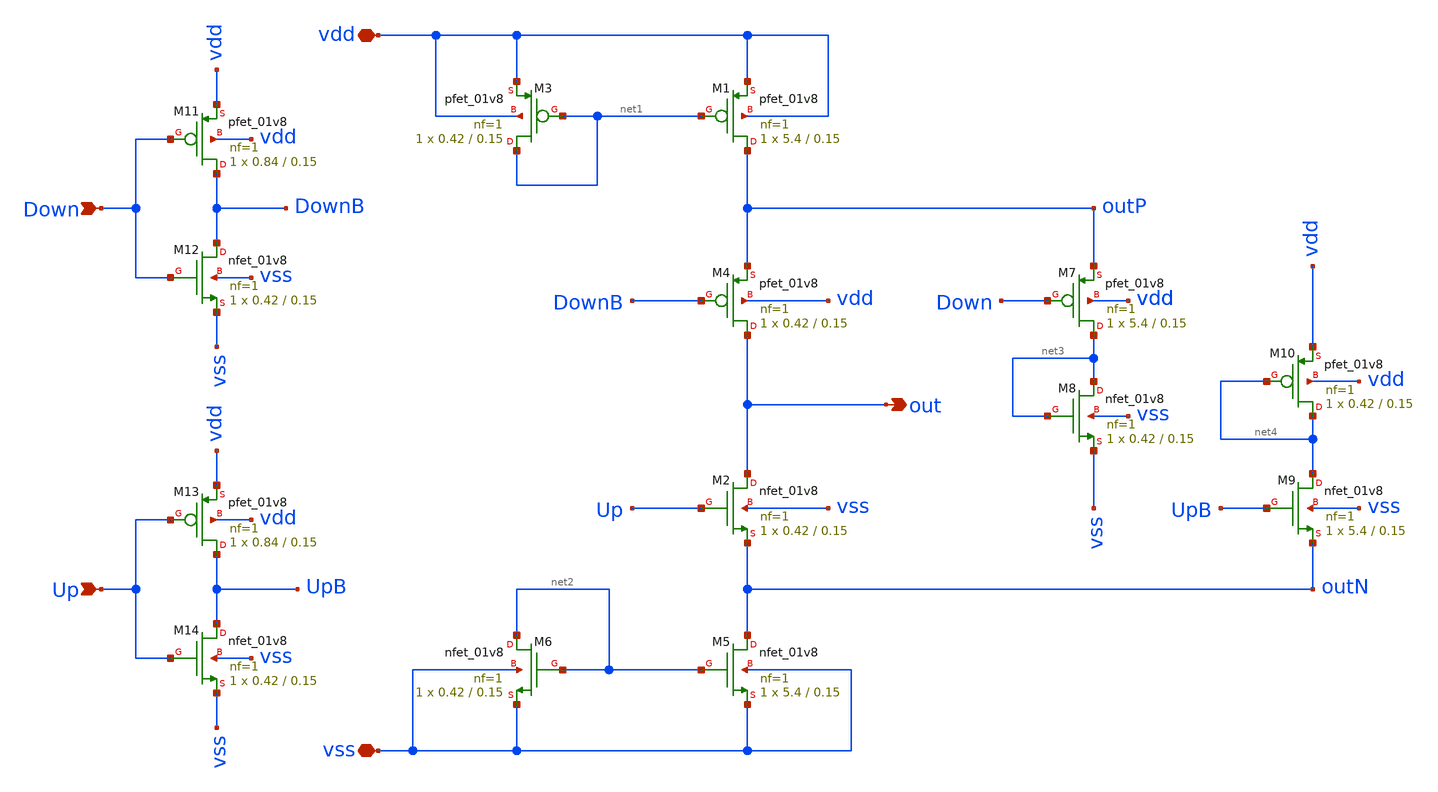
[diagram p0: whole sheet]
** sch_path: sch/PLL_caravel/CP.sch
**.subckt CP vdd Down out vss Up
*.iopin vdd
*.ipin Down
*.opin out
*.iopin vss
*.ipin Up
XM1 outP net1 vdd vdd sky130_fd_pr__pfet_01v8 L=0.15 W=5.4 nf=1 ad='int((nf+1)/2) * W/nf * 0.29' as='int((nf+2)/2) * W/nf * 0.29'
+ pd='2*int((nf+1)/2) * (W/nf + 0.29)' ps='2*int((nf+2)/2) * (W/nf + 0.29)' nrd='0.29 / W' nrs='0.29 / W'
+ sa=0 sb=0 sd=0 mult=1 m=1
XM2 out Up outN vss sky130_fd_pr__nfet_01v8 L=0.15 W=0.42 nf=1 ad='int((nf+1)/2) * W/nf * 0.29' as='int((nf+2)/2) * W/nf * 0.29'
+ pd='2*int((nf+1)/2) * (W/nf + 0.29)' ps='2*int((nf+2)/2) * (W/nf + 0.29)' nrd='0.29 / W' nrs='0.29 / W'
+ sa=0 sb=0 sd=0 mult=1 m=1
XM3 net1 net1 vdd vdd sky130_fd_pr__pfet_01v8 L=0.15 W=0.42 nf=1 ad='int((nf+1)/2) * W/nf * 0.29' as='int((nf+2)/2) * W/nf * 0.29'
+ pd='2*int((nf+1)/2) * (W/nf + 0.29)' ps='2*int((nf+2)/2) * (W/nf + 0.29)' nrd='0.29 / W' nrs='0.29 / W'
+ sa=0 sb=0 sd=0 mult=1 m=1
XM4 out DownB outP vdd sky130_fd_pr__pfet_01v8 L=0.15 W=0.42 nf=1 ad='int((nf+1)/2) * W/nf * 0.29' as='int((nf+2)/2) * W/nf * 0.29'
+ pd='2*int((nf+1)/2) * (W/nf + 0.29)' ps='2*int((nf+2)/2) * (W/nf + 0.29)' nrd='0.29 / W' nrs='0.29 / W'
+ sa=0 sb=0 sd=0 mult=1 m=1
XM5 outN net2 vss vss sky130_fd_pr__nfet_01v8 L=0.15 W=5.4 nf=1 ad='int((nf+1)/2) * W/nf * 0.29' as='int((nf+2)/2) * W/nf * 0.29'
+ pd='2*int((nf+1)/2) * (W/nf + 0.29)' ps='2*int((nf+2)/2) * (W/nf + 0.29)' nrd='0.29 / W' nrs='0.29 / W'
+ sa=0 sb=0 sd=0 mult=1 m=1
XM6 net2 net2 vss vss sky130_fd_pr__nfet_01v8 L=0.15 W=0.42 nf=1 ad='int((nf+1)/2) * W/nf * 0.29' as='int((nf+2)/2) * W/nf * 0.29'
+ pd='2*int((nf+1)/2) * (W/nf + 0.29)' ps='2*int((nf+2)/2) * (W/nf + 0.29)' nrd='0.29 / W' nrs='0.29 / W'
+ sa=0 sb=0 sd=0 mult=1 m=1
XM7 net3 Down outP vdd sky130_fd_pr__pfet_01v8 L=0.15 W=5.4 nf=1 ad='int((nf+1)/2) * W/nf * 0.29' as='int((nf+2)/2) * W/nf * 0.29'
+ pd='2*int((nf+1)/2) * (W/nf + 0.29)' ps='2*int((nf+2)/2) * (W/nf + 0.29)' nrd='0.29 / W' nrs='0.29 / W'
+ sa=0 sb=0 sd=0 mult=1 m=1
XM8 net3 net3 vss vss sky130_fd_pr__nfet_01v8 L=0.15 W=0.42 nf=1 ad='int((nf+1)/2) * W/nf * 0.29' as='int((nf+2)/2) * W/nf * 0.29'
+ pd='2*int((nf+1)/2) * (W/nf + 0.29)' ps='2*int((nf+2)/2) * (W/nf + 0.29)' nrd='0.29 / W' nrs='0.29 / W'
+ sa=0 sb=0 sd=0 mult=1 m=1
XM9 net4 UpB outN vss sky130_fd_pr__nfet_01v8 L=0.15 W=5.4 nf=1 ad='int((nf+1)/2) * W/nf * 0.29' as='int((nf+2)/2) * W/nf * 0.29'
+ pd='2*int((nf+1)/2) * (W/nf + 0.29)' ps='2*int((nf+2)/2) * (W/nf + 0.29)' nrd='0.29 / W' nrs='0.29 / W'
+ sa=0 sb=0 sd=0 mult=1 m=1
XM10 net4 net4 vdd vdd sky130_fd_pr__pfet_01v8 L=0.15 W=0.42 nf=1 ad='int((nf+1)/2) * W/nf * 0.29' as='int((nf+2)/2) * W/nf * 0.29'
+ pd='2*int((nf+1)/2) * (W/nf + 0.29)' ps='2*int((nf+2)/2) * (W/nf + 0.29)' nrd='0.29 / W' nrs='0.29 / W'
+ sa=0 sb=0 sd=0 mult=1 m=1
XM11 DownB Down vdd vdd sky130_fd_pr__pfet_01v8 L=0.15 W=0.84 nf=1 ad='int((nf+1)/2) * W/nf * 0.29' as='int((nf+2)/2) * W/nf * 0.29'
+ pd='2*int((nf+1)/2) * (W/nf + 0.29)' ps='2*int((nf+2)/2) * (W/nf + 0.29)' nrd='0.29 / W' nrs='0.29 / W'
+ sa=0 sb=0 sd=0 mult=1 m=1
XM12 DownB Down vss vss sky130_fd_pr__nfet_01v8 L=0.15 W=0.42 nf=1 ad='int((nf+1)/2) * W/nf * 0.29' as='int((nf+2)/2) * W/nf * 0.29'
+ pd='2*int((nf+1)/2) * (W/nf + 0.29)' ps='2*int((nf+2)/2) * (W/nf + 0.29)' nrd='0.29 / W' nrs='0.29 / W'
+ sa=0 sb=0 sd=0 mult=1 m=1
XM13 UpB Up vdd vdd sky130_fd_pr__pfet_01v8 L=0.15 W=0.84 nf=1 ad='int((nf+1)/2) * W/nf * 0.29' as='int((nf+2)/2) * W/nf * 0.29'
+ pd='2*int((nf+1)/2) * (W/nf + 0.29)' ps='2*int((nf+2)/2) * (W/nf + 0.29)' nrd='0.29 / W' nrs='0.29 / W'
+ sa=0 sb=0 sd=0 mult=1 m=1
XM14 UpB Up vss vss sky130_fd_pr__nfet_01v8 L=0.15 W=0.42 nf=1 ad='int((nf+1)/2) * W/nf * 0.29' as='int((nf+2)/2) * W/nf * 0.29'
+ pd='2*int((nf+1)/2) * (W/nf + 0.29)' ps='2*int((nf+2)/2) * (W/nf + 0.29)' nrd='0.29 / W' nrs='0.29 / W'
+ sa=0 sb=0 sd=0 mult=1 m=1
**.ends
.end
